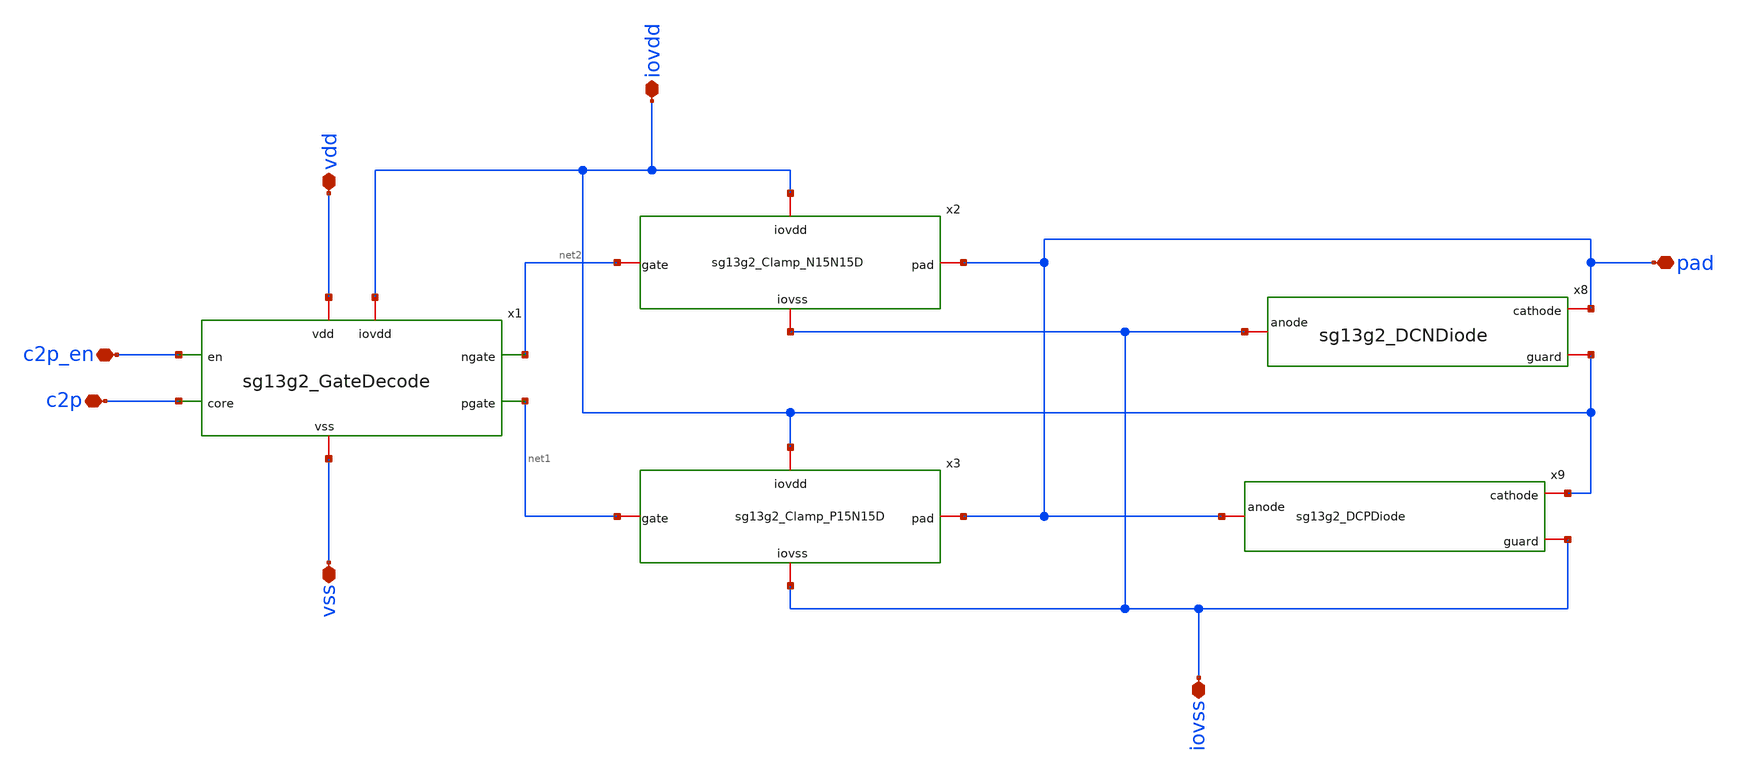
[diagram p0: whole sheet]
** sch_path: CDR4176-main/schematic/xschem/project_io/sg13g2_IOPadTriOut30mA/sg13g2_IOPadTriOut30mA.sch
**.subckt sg13g2_IOPadTriOut30mA iovss pad vss c2p vdd iovdd c2p_en
*.iopin iovss
*.iopin pad
*.iopin vss
*.iopin c2p
*.iopin vdd
*.iopin iovdd
*.iopin c2p_en
x8 pad iovss iovdd sg13g2_DCNDiode
x9 iovdd pad iovss sg13g2_DCPDiode
x1 vdd iovdd c2p_en net2 net1 c2p vss sg13g2_GateDecode
x2 iovdd pad net2 iovss sg13g2_Clamp_N15N15D
x3 iovdd net1 pad iovss sg13g2_Clamp_P15N15D
**.ends
.end
